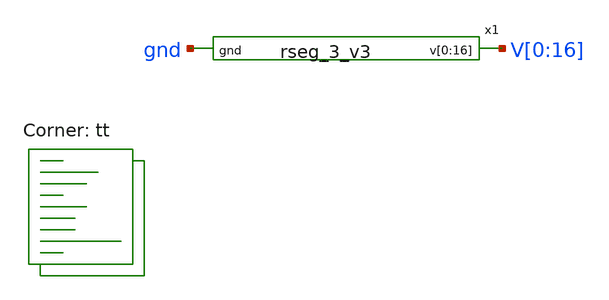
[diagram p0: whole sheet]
** sch_path: xschem/rseg_3_v3-tb.sch
**.subckt rseg_3_v3-tb
x1 V[0] V[1] V[2] V[3] V[4] V[5] V[6] V[7] V[8] V[9] V[10] V[11] V[12] V[13] V[14] V[15] V[16] gnd
+ rseg_3_v3
**** begin user architecture code



  .include $THESIS_WS/spice/header.spice

  .option wnflag=1
  .option safecurrents

  V16 v[16] gnd dc 4.7190
  v0 v[0] gnd dc 4.0164
  vd vd gnd 0

  .control
     reset
     save all
     dc vd 0 1 1
     write rseg_3_v3-tb.raw
     set appendwrite

*    quit 0
  .endc



.lib $::SKYWATER_MODELS/sky130.lib.spice tt
**** end user architecture code
**.ends
.end
